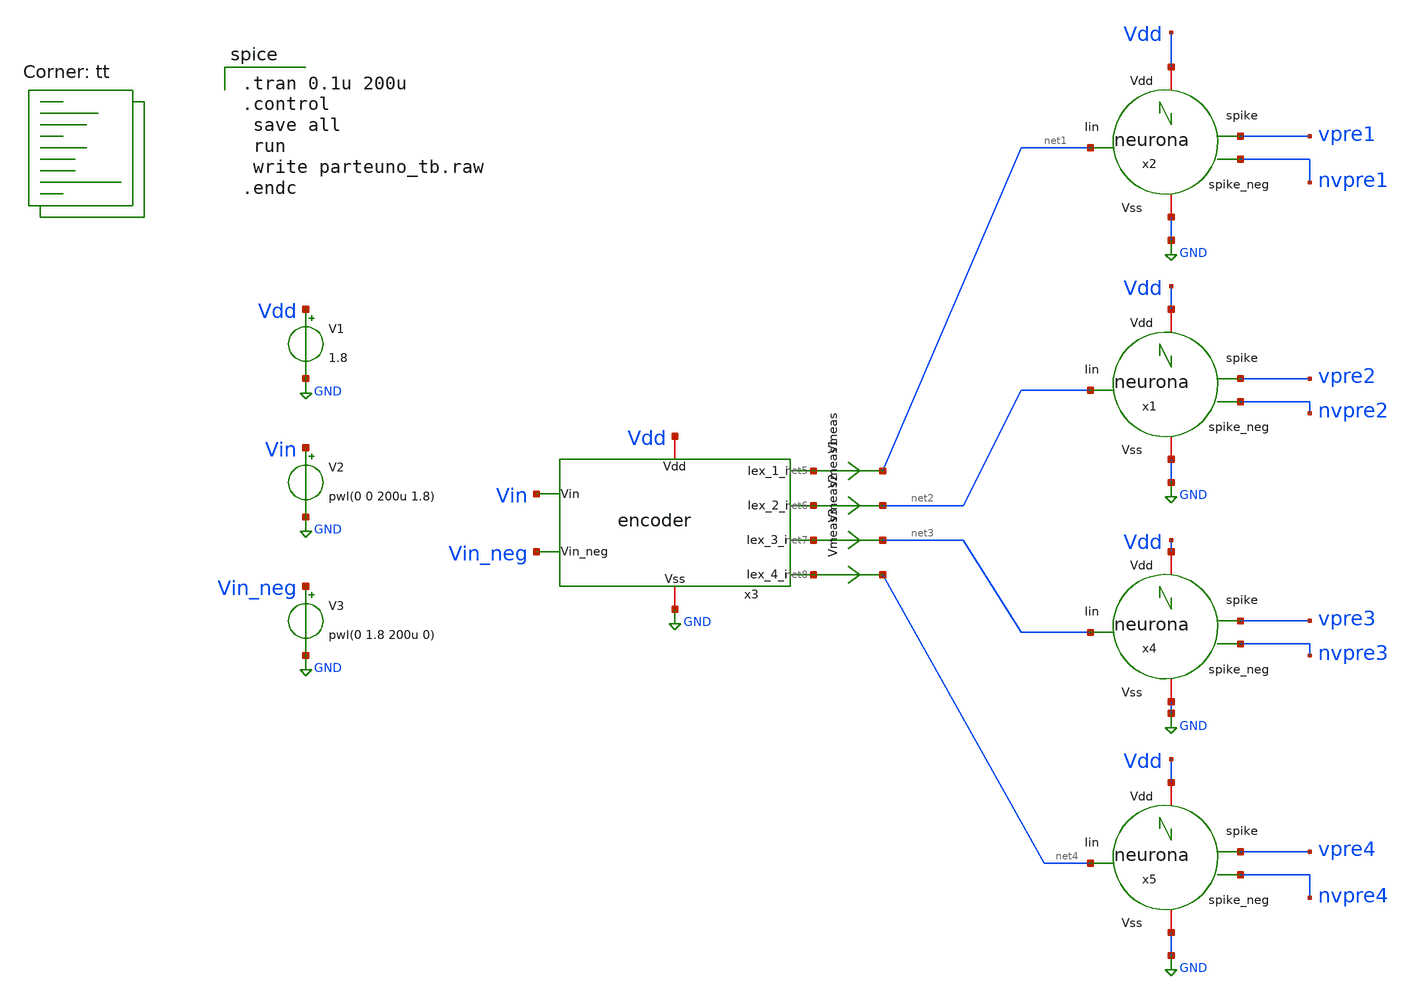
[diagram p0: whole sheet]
** sch_path: designs/libs/snn_analog/encoder/parteuno_tb.sch
**.subckt parteuno_tb
x2 net1 Vdd GND vpre1 nvpre1 neurona
V1 Vdd GND 1.8
V2 Vin GND pwl(0 0 200u 1.8)
V3 Vin_neg GND pwl(0 1.8 200u 0)
Vmeas net5 net1 0
.save i(vmeas)
Vmeas1 net6 net2 0
.save i(vmeas1)
Vmeas2 net7 net3 0
.save i(vmeas2)
Vmeas3 net8 net4 0
.save i(vmeas3)
x3 Vdd GND Vin Vin_neg net5 net6 net7 net8 encoder
x1 net2 Vdd GND vpre2 nvpre2 neurona
x4 net3 Vdd GND vpre3 nvpre3 neurona
x5 net4 Vdd GND vpre4 nvpre4 neurona
**** begin user architecture code

.tran 0.1u 200u
.control
 save all
 run
 write parteuno_tb.raw
.endc

.lib $::SKYWATER_MODELS/sky130.lib.spice tt
**** end user architecture code
**.ends

* expanding   symbol:  libs/snn_analog/lif/sch/lif/neurona.sym # of pins=5
** sym_path: designs/libs/snn_analog/lif/sch/neurona.sym
** sch_path: designs/libs/snn_analog/lif/sch/neurona.sch
.subckt neurona Iin Vdd Vss spike spike_neg
*.iopin Vdd
*.iopin Vss
*.ipin Iin
*.opin spike
*.opin spike_neg
XM2 spike_neg Iin Vss Vss sky130_fd_pr__nfet_01v8 L=0.28 W=0.5 nf=1 ad='int((1 + 1)/2) * 0.5 / 1 * 0.29'
+ as='int((1 + 2)/2) * 0.5 / 1 * 0.29' pd='2*int((1 + 1)/2) * (0.5 / 1 + 0.29)' ps='2*int((1 + 2)/2) * (0.5 / 1 + 0.29)'
+ nrd='0.29 / 0.5 ' nrs='0.29 / 0.5 ' sa=0 sb=0 sd=0 mult=1 m=1
XM1 spike_neg Iin Vdd Vdd sky130_fd_pr__pfet_01v8 L=0.28 W=0.5 nf=1 ad='int((1 + 1)/2) * 0.5 / 1 * 0.29'
+ as='int((1 + 2)/2) * 0.5 / 1 * 0.29' pd='2*int((1 + 1)/2) * (0.5 / 1 + 0.29)' ps='2*int((1 + 2)/2) * (0.5 / 1 + 0.29)'
+ nrd='0.29 / 0.5 ' nrs='0.29 / 0.5 ' sa=0 sb=0 sd=0 mult=1 m=1
XM3 spike/reset spike_neg Vdd Vdd sky130_fd_pr__pfet_01v8 L=0.28 W=0.5 nf=1 ad='int((1 + 1)/2) * 0.5 / 1 * 0.29'
+ as='int((1 + 2)/2) * 0.5 / 1 * 0.29' pd='2*int((1 + 1)/2) * (0.5 / 1 + 0.29)' ps='2*int((1 + 2)/2) * (0.5 / 1 + 0.29)'
+ nrd='0.29 / 0.5 ' nrs='0.29 / 0.5 ' sa=0 sb=0 sd=0 mult=1 m=1
XM4 spike/reset spike_neg Vss Vss sky130_fd_pr__nfet_01v8 L=0.28 W=0.5 nf=1 ad='int((1 + 1)/2) * 0.5 / 1 * 0.29'
+ as='int((1 + 2)/2) * 0.5 / 1 * 0.29' pd='2*int((1 + 1)/2) * (0.5 / 1 + 0.29)' ps='2*int((1 + 2)/2) * (0.5 / 1 + 0.29)'
+ nrd='0.29 / 0.5 ' nrs='0.29 / 0.5 ' sa=0 sb=0 sd=0 mult=1 m=1
XM5 Iin spike/reset Vss Vss sky130_fd_pr__nfet_01v8 L=20 W=3 nf=1 ad='int((1 + 1)/2) * 3 / 1 * 0.29'
+ as='int((1 + 2)/2) * 3 / 1 * 0.29' pd='2*int((1 + 1)/2) * (3 / 1 + 0.29)' ps='2*int((1 + 2)/2) * (3 / 1 + 0.29)'
+ nrd='0.29 / 3 ' nrs='0.29 / 3 ' sa=0 sb=0 sd=0 mult=1 m=1
XM6 spike spike_neg Vdd Vdd sky130_fd_pr__pfet_01v8 L=0.28 W=0.5 nf=1 ad='int((1 + 1)/2) * 0.5 / 1 * 0.29'
+ as='int((1 + 2)/2) * 0.5 / 1 * 0.29' pd='2*int((1 + 1)/2) * (0.5 / 1 + 0.29)' ps='2*int((1 + 2)/2) * (0.5 / 1 + 0.29)'
+ nrd='0.29 / 0.5 ' nrs='0.29 / 0.5 ' sa=0 sb=0 sd=0 mult=1 m=1
XM7 spike spike_neg Vss Vss sky130_fd_pr__nfet_01v8 L=0.28 W=0.5 nf=1 ad='int((1 + 1)/2) * 0.5 / 1 * 0.29'
+ as='int((1 + 2)/2) * 0.5 / 1 * 0.29' pd='2*int((1 + 1)/2) * (0.5 / 1 + 0.29)' ps='2*int((1 + 2)/2) * (0.5 / 1 + 0.29)'
+ nrd='0.29 / 0.5 ' nrs='0.29 / 0.5 ' sa=0 sb=0 sd=0 mult=1 m=1
XC1 Iin Vss sky130_fd_pr__cap_mim_m3_1 W=15 L=5 MF=1 m=1
.ends


* expanding   symbol:  libs/snn_analog/encoder/sch/encoder.sym # of pins=8
** sym_path: designs/libs/snn_analog/encoder/sch/encoder.sym
** sch_path: designs/libs/snn_analog/encoder/sch/encoder.sch
.subckt encoder Vdd Vss Vin Vin_neg Iex_1_i Iex_2_i Iex_3_i Iex_4_i
*.iopin Vdd
*.iopin Vss
*.ipin Vin
*.ipin Vin_neg
*.opin Iex_1_i
*.opin Iex_4_i
*.opin Iex_2_i
*.opin Iex_3_i
XM1 x Vin a Vss sky130_fd_pr__nfet_01v8 L=10 W=0.5 nf=1 ad='int((1 + 1)/2) * 0.5 / 1 * 0.29' as='int((1 + 2)/2) * 0.5 / 1 * 0.29'
+ pd='2*int((1 + 1)/2) * (0.5 / 1 + 0.29)' ps='2*int((1 + 2)/2) * (0.5 / 1 + 0.29)' nrd='0.29 / 0.5 ' nrs='0.29 / 0.5 '
+ sa=0 sb=0 sd=0 mult=1 m=1
XM2 y Vin_neg a Vss sky130_fd_pr__nfet_01v8 L=10 W=0.5 nf=1 ad='int((1 + 1)/2) * 0.5 / 1 * 0.29' as='int((1 + 2)/2) * 0.5 / 1 * 0.29'
+ pd='2*int((1 + 1)/2) * (0.5 / 1 + 0.29)' ps='2*int((1 + 2)/2) * (0.5 / 1 + 0.29)' nrd='0.29 / 0.5 ' nrs='0.29 / 0.5 '
+ sa=0 sb=0 sd=0 mult=1 m=1
XM3 x x Vdd Vdd sky130_fd_pr__pfet_01v8 L=0.28 W=2 nf=1 ad='int((1 + 1)/2) * 2 / 1 * 0.29' as='int((1 + 2)/2) * 2 / 1 * 0.29'
+ pd='2*int((1 + 1)/2) * (2 / 1 + 0.29)' ps='2*int((1 + 2)/2) * (2 / 1 + 0.29)' nrd='0.29 / 2 ' nrs='0.29 / 2 '
+ sa=0 sb=0 sd=0 mult=1 m=1
XM4 y y Vdd Vdd sky130_fd_pr__pfet_01v8 L=0.28 W=2 nf=1 ad='int((1 + 1)/2) * 2 / 1 * 0.29' as='int((1 + 2)/2) * 2 / 1 * 0.29'
+ pd='2*int((1 + 1)/2) * (2 / 1 + 0.29)' ps='2*int((1 + 2)/2) * (2 / 1 + 0.29)' nrd='0.29 / 2 ' nrs='0.29 / 2 '
+ sa=0 sb=0 sd=0 mult=1 m=1
XM5 Iex_2_i x Vdd Vdd sky130_fd_pr__pfet_01v8 L=0.94 W=0.5 nf=1 ad='int((1 + 1)/2) * 0.5 / 1 * 0.29'
+ as='int((1 + 2)/2) * 0.5 / 1 * 0.29' pd='2*int((1 + 1)/2) * (0.5 / 1 + 0.29)' ps='2*int((1 + 2)/2) * (0.5 / 1 + 0.29)'
+ nrd='0.29 / 0.5 ' nrs='0.29 / 0.5 ' sa=0 sb=0 sd=0 mult=1 m=1
XM6 Iex_4_i y Vdd Vdd sky130_fd_pr__pfet_01v8 L=0.94 W=0.5 nf=1 ad='int((1 + 1)/2) * 0.5 / 1 * 0.29'
+ as='int((1 + 2)/2) * 0.5 / 1 * 0.29' pd='2*int((1 + 1)/2) * (0.5 / 1 + 0.29)' ps='2*int((1 + 2)/2) * (0.5 / 1 + 0.29)'
+ nrd='0.29 / 0.5 ' nrs='0.29 / 0.5 ' sa=0 sb=0 sd=0 mult=1 m=1
XM7 Iex_3_i y Vdd Vdd sky130_fd_pr__pfet_01v8 L=0.94 W=0.5 nf=1 ad='int((1 + 1)/2) * 0.5 / 1 * 0.29'
+ as='int((1 + 2)/2) * 0.5 / 1 * 0.29' pd='2*int((1 + 1)/2) * (0.5 / 1 + 0.29)' ps='2*int((1 + 2)/2) * (0.5 / 1 + 0.29)'
+ nrd='0.29 / 0.5 ' nrs='0.29 / 0.5 ' sa=0 sb=0 sd=0 mult=1 m=1
XM8 Iex_1_i x Vdd Vdd sky130_fd_pr__pfet_01v8 L=0.94 W=0.5 nf=1 ad='int((1 + 1)/2) * 0.5 / 1 * 0.29'
+ as='int((1 + 2)/2) * 0.5 / 1 * 0.29' pd='2*int((1 + 1)/2) * (0.5 / 1 + 0.29)' ps='2*int((1 + 2)/2) * (0.5 / 1 + 0.29)'
+ nrd='0.29 / 0.5 ' nrs='0.29 / 0.5 ' sa=0 sb=0 sd=0 mult=1 m=1
XM9 a net1 Vss Vss sky130_fd_pr__nfet_01v8 L=1.12 W=2 nf=1 ad='int((1 + 1)/2) * 2 / 1 * 0.29' as='int((1 + 2)/2) * 2 / 1 * 0.29'
+ pd='2*int((1 + 1)/2) * (2 / 1 + 0.29)' ps='2*int((1 + 2)/2) * (2 / 1 + 0.29)' nrd='0.29 / 2 ' nrs='0.29 / 2 '
+ sa=0 sb=0 sd=0 mult=1 m=1
XM10 net1 net1 Vss Vss sky130_fd_pr__nfet_01v8 L=0.28 W=0.5 nf=1 ad='int((1 + 1)/2) * 0.5 / 1 * 0.29'
+ as='int((1 + 2)/2) * 0.5 / 1 * 0.29' pd='2*int((1 + 1)/2) * (0.5 / 1 + 0.29)' ps='2*int((1 + 2)/2) * (0.5 / 1 + 0.29)'
+ nrd='0.29 / 0.5 ' nrs='0.29 / 0.5 ' sa=0 sb=0 sd=0 mult=1 m=1
XM11 net1 net1 Vdd Vdd sky130_fd_pr__pfet_01v8 L=0.28 W=0.5 nf=1 ad='int((1 + 1)/2) * 0.5 / 1 * 0.29'
+ as='int((1 + 2)/2) * 0.5 / 1 * 0.29' pd='2*int((1 + 1)/2) * (0.5 / 1 + 0.29)' ps='2*int((1 + 2)/2) * (0.5 / 1 + 0.29)'
+ nrd='0.29 / 0.5 ' nrs='0.29 / 0.5 ' sa=0 sb=0 sd=0 mult=1 m=1
.ends

.GLOBAL GND
.end
